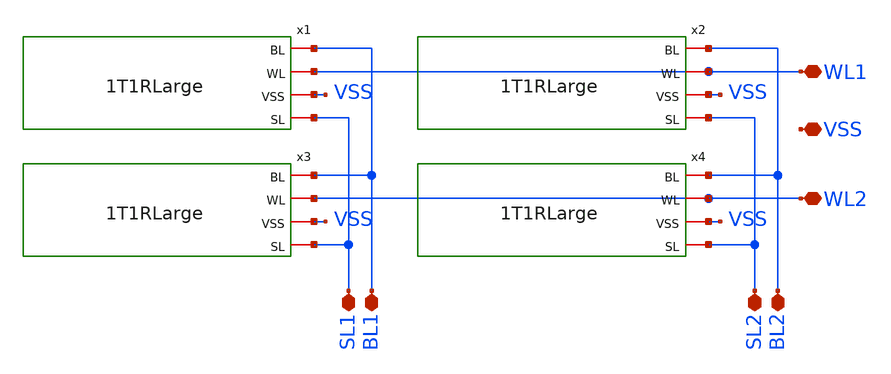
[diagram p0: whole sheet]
** sch_path: xschem/4T4RLarge.sch
* StefanSchippers/xschem_sky130/sky130_fd_pr/reram.sym:
* Copyright 2021 Stefan Frederik Schippers
* Licensed under the Apache License, Version 2.0 (the "License");
**.subckt 4T4RLarge WL1 BL1 WL2 BL2 SL1 SL2 VSS
*.iopin WL1
*.iopin BL1
*.iopin WL2
*.iopin BL2
*.iopin SL1
*.iopin SL2
*.iopin VSS
x1 BL1 WL1 VSS SL1 1T1RLarge
x2 BL2 WL1 VSS SL2 1T1RLarge
x3 BL1 WL2 VSS SL1 1T1RLarge
x4 BL2 WL2 VSS SL2 1T1RLarge
**.ends

* expanding   symbol:  1T1RLarge.sym # of pins=4
** sym_path: xschem/1T1RLarge.sym
** sch_path: xschem/1T1RLarge.sch
.subckt 1T1RLarge BL WL VSS SL
*.iopin SL
*.iopin VSS
*.iopin WL
*.iopin BL
XR1 BL net1 sky130_fd_pr_reram__reram_cell Tfilament_0=3.8e-9
XM1 net1 WL SL VSS sky130_fd_pr__nfet_g5v0d10v5 L=0.5 W=14 nf=1 ad='int((nf+1)/2) * W/nf * 0.29' as='int((nf+2)/2) * W/nf * 0.29'
+ pd='2*int((nf+1)/2) * (W/nf + 0.29)' ps='2*int((nf+2)/2) * (W/nf + 0.29)' nrd='0.29 / W' nrs='0.29 / W'
+ sa=0 sb=0 sd=0 mult=1 m=1
.ends

**** begin user architecture code

.subckt sky130_fd_pr_reram__reram_cell TE BE Tfilament_0=3.3e-9 area_ox=0.1024e-12
N1 TE BE nFilament sky130_fd_pr_reram__reram_model
.ic v(nFilament)={Tfilament_0*1.0e9}
.ends sky130_fd_pr_reram__reram_cell

.model sky130_fd_pr_reram__reram_model sky130_fd_pr_reram__reram_module  area_ox = 0.1024e-12  Tox =
+ 5.0  Tfilament_max = 4.9  Tfilament_min = 3.3  Eact_generation = 1.501  Eact_recombination  = 1.500
+  I_k1  = 6.140e-5  Tfilament_ref = 4.7249  V_ref = 0.430  velocity_k1 = 150  gamma_k0  = 16.5  gamma_k1
+  = -1.25  Temperature_0 = 300  C_thermal = 3.1825e-16  tau_thermal = 0.23e-9  t_step  = 1.0e-9
+  smoothing = 1e-7  Kclip = 200

.control
pre_osdi $SKYWATER_MODELS/sky130_fd_pr_reram__reram_module.osdi
.endc

**** end user architecture code
.end
